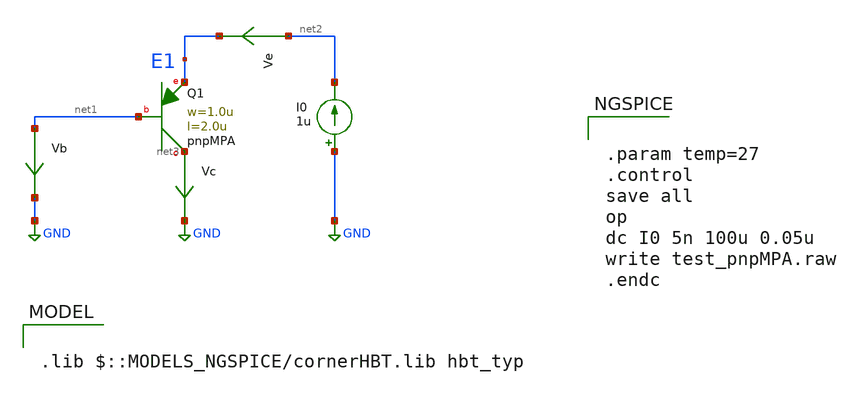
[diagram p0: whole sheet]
** sch_path: ihp-sg13g2/libs.tech/xschem/sg13g2_tests_xyce/dc_pnpMPA.sch
* Copyright 2023 IHP PDK Authors
**.subckt dc_pnpMPA
XQ1 net3 net1 E1 pnpMPA a=2p p=6u m=1
Ve net2 E1 0
.save i(ve)
Vb net1 GND 0
.save i(vb)
Vc net3 GND 0
.save i(vc)
I0 GND net2 1u
**** begin user architecture code

.lib $::MODELS_NGSPICE/cornerHBT.lib hbt_typ



.param temp=27
.control
save all
op
dc I0 5n 100u 0.05u
write test_pnpMPA.raw
.endc


**** end user architecture code
**.ends
.GLOBAL GND
.end
